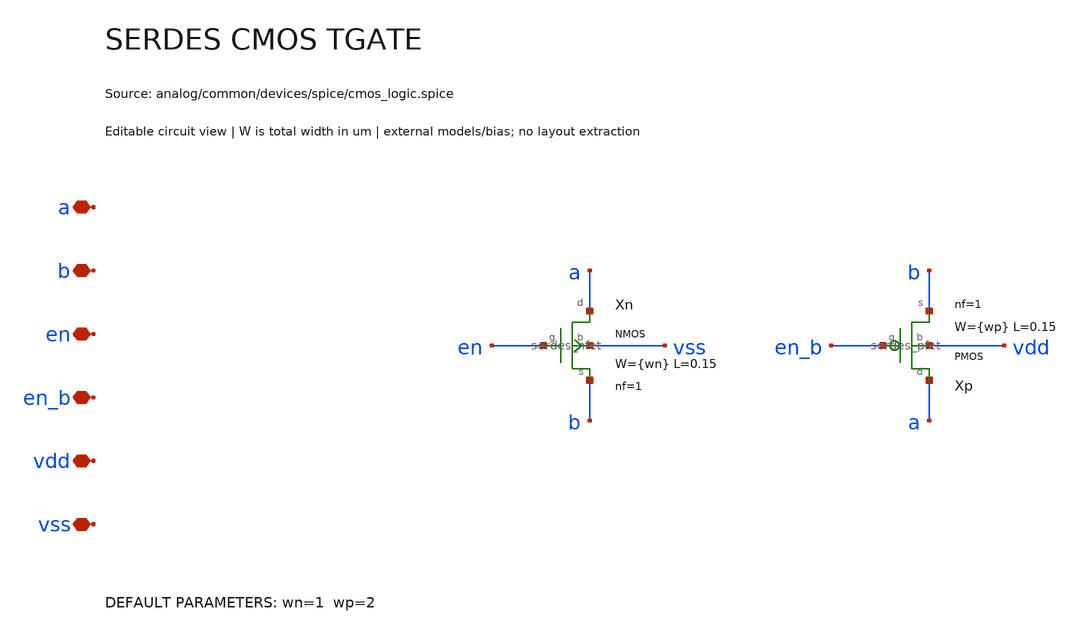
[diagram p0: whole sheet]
** sch_path: analog/common/devices/schematic/serdes_cmos_tgate.sch
**.subckt serdes_cmos_tgate a b en en_b vdd vss
*.iopin a
*.iopin b
*.iopin en
*.iopin en_b
*.iopin vdd
*.iopin vss
Xn a en b vss serdes_nfet w={wn} l=0.15 nf=1
Xp a en_b b vdd serdes_pfet w={wp} l=0.15 nf=1
**.ends

* expanding   symbol:  serdes/serdes_nfet.sym # of pins=4
** sym_path: analog/common/devices/schematic/serdes_nfet.sym
** sch_path: analog/common/devices/schematic/serdes_nfet.sch
.subckt serdes_nfet d g s b  w=1 l=0.15 nf=1
*.iopin d
*.iopin g
*.iopin s
*.iopin b
Xmos d g s b sky130_fd_pr__nfet_01v8 w={w} l={l} nf={nf} ad={floor((nf+1)/2)*(w/nf)*0.29} as={floor((nf+2)/2)*(w/nf)*0.29}
+ pd={2*floor((nf+1)/2)*(w/nf+0.29)} ps={2*floor((nf+2)/2)*(w/nf+0.29)}
.ends


* expanding   symbol:  serdes/serdes_pfet.sym # of pins=4
** sym_path: analog/common/devices/schematic/serdes_pfet.sym
** sch_path: analog/common/devices/schematic/serdes_pfet.sch
.subckt serdes_pfet d g s b  w=3 l=0.15 nf=1
*.iopin d
*.iopin g
*.iopin s
*.iopin b
Xmos d g s b sky130_fd_pr__pfet_01v8 w={w} l={l} nf={nf} ad={floor((nf+1)/2)*(w/nf)*0.29} as={floor((nf+2)/2)*(w/nf)*0.29}
+ pd={2*floor((nf+1)/2)*(w/nf+0.29)} ps={2*floor((nf+2)/2)*(w/nf+0.29)}
.ends

.end
